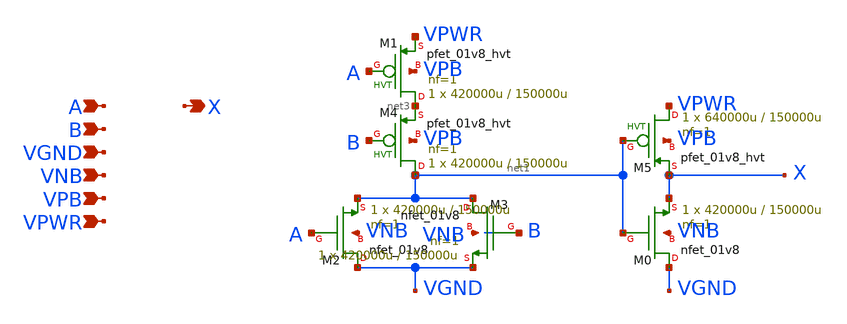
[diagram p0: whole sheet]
** sch_path: schematics/or2/sky130_fd_sc_hd__or2_0.sch
**.subckt sky130_fd_sc_hd__or2_0 A X B VGND VNB VPB VPWR
*.ipin A
*.opin X
*.ipin B
*.ipin VGND
*.ipin VNB
*.ipin VPB
*.ipin VPWR
XM0 VGND net1 X VNB sky130_fd_pr__nfet_01v8 L=150000u W=420000u nf=1 ad='int((1 + 1)/2) * 420000u / 1 * 0.29'
+ as='int((1 + 2)/2) * 420000u / 1 * 0.29' pd='2*int((1 + 1)/2) * (420000u / 1 + 0.29)' ps='2*int((1 + 2)/2) * (420000u / 1 + 0.29)'
+ nrd='0.29 / 420000u ' nrs='0.29 / 420000u ' sa=0 sb=0 sd=0 mult=1 m=1
XM1 net3 A VPWR VPB sky130_fd_pr__pfet_01v8_hvt L=150000u W=420000u nf=1 ad='int((1 + 1)/2) * 420000u / 1 * 0.29'
+ as='int((1 + 2)/2) * 420000u / 1 * 0.29' pd='2*int((1 + 1)/2) * (420000u / 1 + 0.29)' ps='2*int((1 + 2)/2) * (420000u / 1 + 0.29)'
+ nrd='0.29 / 420000u ' nrs='0.29 / 420000u ' sa=0 sb=0 sd=0 mult=1 m=1
XM2 VGND A net1 VNB sky130_fd_pr__nfet_01v8 L=150000u W=420000u nf=1 ad='int((1 + 1)/2) * 420000u / 1 * 0.29'
+ as='int((1 + 2)/2) * 420000u / 1 * 0.29' pd='2*int((1 + 1)/2) * (420000u / 1 + 0.29)' ps='2*int((1 + 2)/2) * (420000u / 1 + 0.29)'
+ nrd='0.29 / 420000u ' nrs='0.29 / 420000u ' sa=0 sb=0 sd=0 mult=1 m=1
XM4 net1 B net3 VPB sky130_fd_pr__pfet_01v8_hvt L=150000u W=420000u nf=1 ad='int((1 + 1)/2) * 420000u / 1 * 0.29'
+ as='int((1 + 2)/2) * 420000u / 1 * 0.29' pd='2*int((1 + 1)/2) * (420000u / 1 + 0.29)' ps='2*int((1 + 2)/2) * (420000u / 1 + 0.29)'
+ nrd='0.29 / 420000u ' nrs='0.29 / 420000u ' sa=0 sb=0 sd=0 mult=1 m=1
XM5 VPWR net1 X VPB sky130_fd_pr__pfet_01v8_hvt L=150000u W=640000u nf=1 ad='int((1 + 1)/2) * 640000u / 1 * 0.29'
+ as='int((1 + 2)/2) * 640000u / 1 * 0.29' pd='2*int((1 + 1)/2) * (640000u / 1 + 0.29)' ps='2*int((1 + 2)/2) * (640000u / 1 + 0.29)'
+ nrd='0.29 / 640000u ' nrs='0.29 / 640000u ' sa=0 sb=0 sd=0 mult=1 m=1
XM3 net1 B VGND VNB sky130_fd_pr__nfet_01v8 L=150000u W=420000u nf=1 ad='int((1 + 1)/2) * 420000u / 1 * 0.29'
+ as='int((1 + 2)/2) * 420000u / 1 * 0.29' pd='2*int((1 + 1)/2) * (420000u / 1 + 0.29)' ps='2*int((1 + 2)/2) * (420000u / 1 + 0.29)'
+ nrd='0.29 / 420000u ' nrs='0.29 / 420000u ' sa=0 sb=0 sd=0 mult=1 m=1
**.ends
.end
